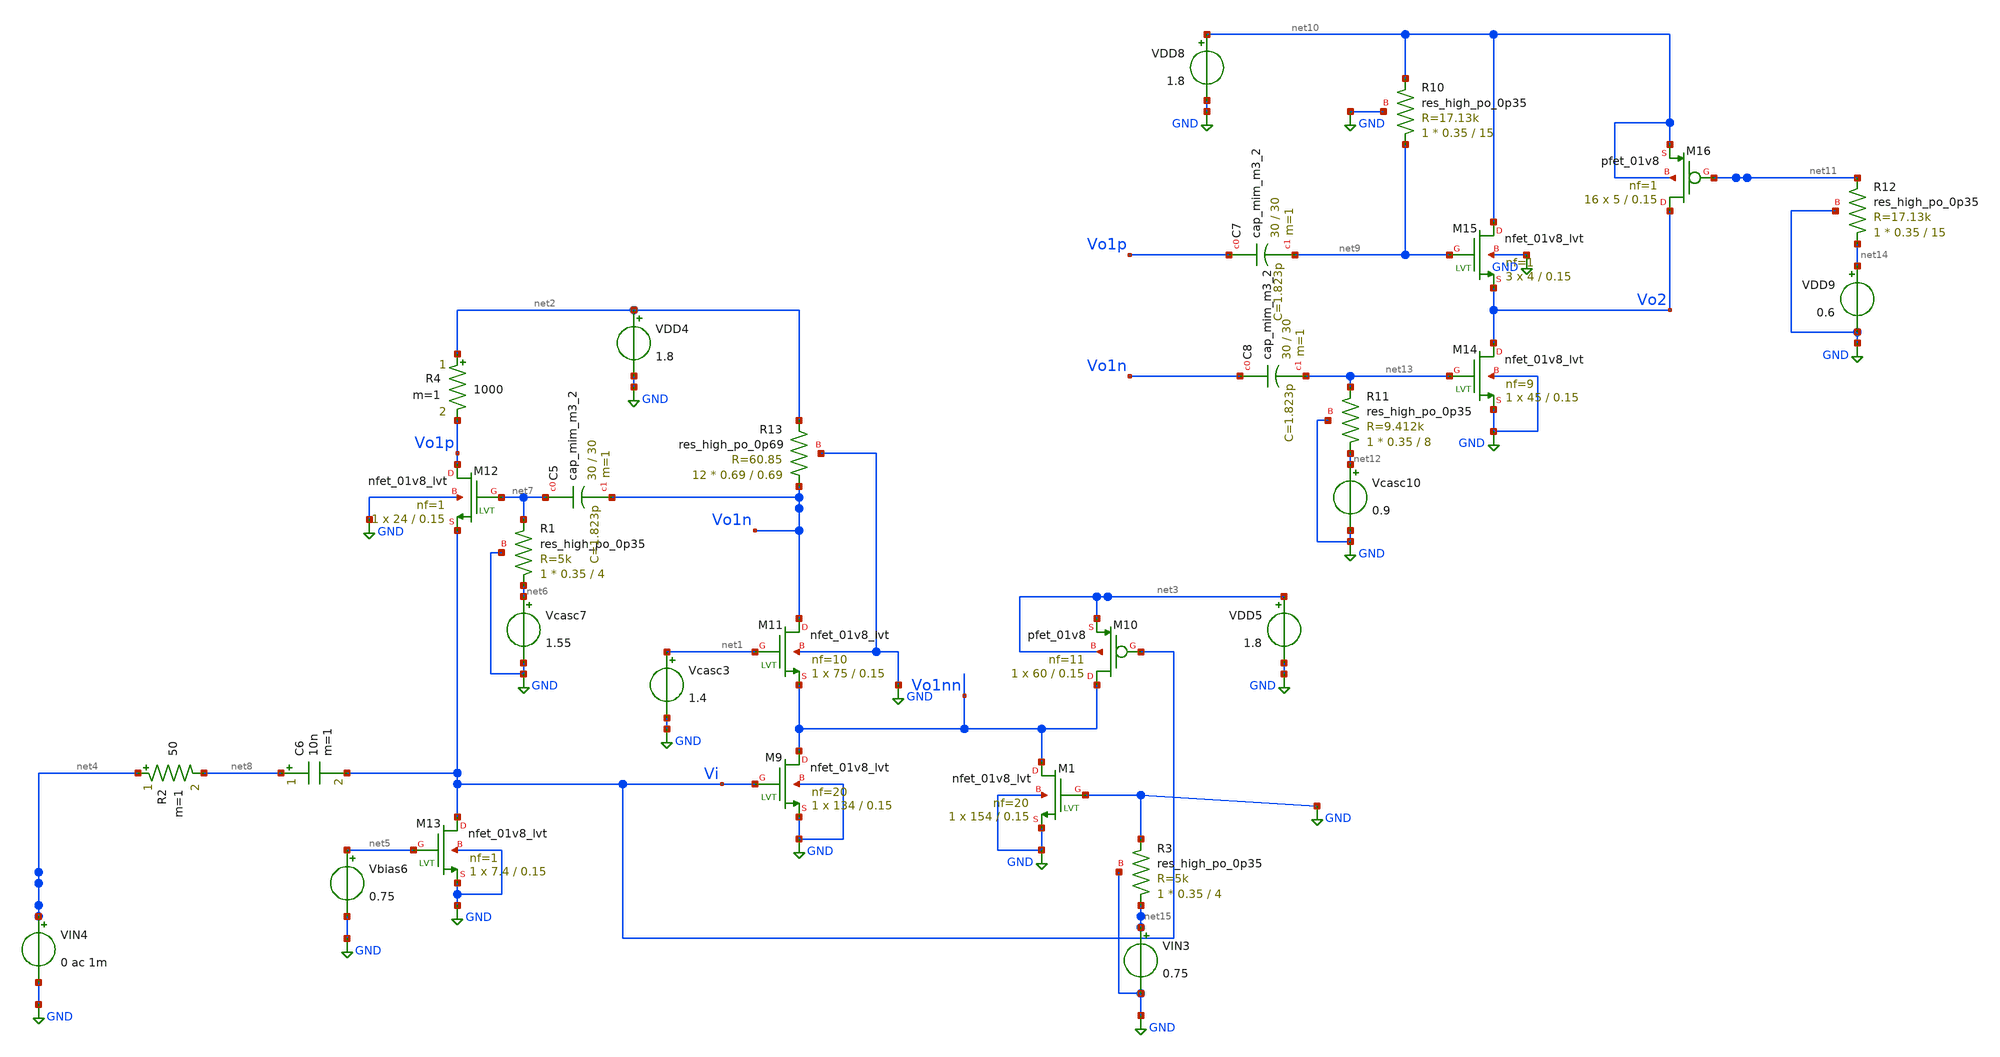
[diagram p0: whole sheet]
** sch_path: xschem/xschem4_sic_final/CompleteAMP6_AC.sch
**.subckt CompleteAMP6_AC
Vcasc3 net1 GND 1.4
VDD4 net2 GND 1.8
VDD5 net3 GND 1.8
Vbias6 net5 GND 0.75
Vcasc7 net6 GND 1.55
XR1 net6 net7 GND sky130_fd_pr__res_high_po_0p35 L=4 mult=1 m=1
XC5 net7 Vo1n sky130_fd_pr__cap_mim_m3_2 W=30 L=30 MF=1 m=1
C6 net8 Vi 10n m=1
XM9 Vo1nn Vi GND GND sky130_fd_pr__nfet_01v8_lvt L=0.15 W=134 nf=20 ad='int((nf+1)/2) * W/nf * 0.29'
+ as='int((nf+2)/2) * W/nf * 0.29' pd='2*int((nf+1)/2) * (W/nf + 0.29)' ps='2*int((nf+2)/2) * (W/nf + 0.29)'
+ nrd='0.29 / W' nrs='0.29 / W' sa=0 sb=0 sd=0 mult=1 m=1
XM10 Vo1nn Vi net3 net3 sky130_fd_pr__pfet_01v8 L=0.15 W=60 nf=11 ad='int((nf+1)/2) * W/nf * 0.29' as='int((nf+2)/2) * W/nf * 0.29'
+ pd='2*int((nf+1)/2) * (W/nf + 0.29)' ps='2*int((nf+2)/2) * (W/nf + 0.29)' nrd='0.29 / W' nrs='0.29 / W'
+ sa=0 sb=0 sd=0 mult=1 m=1
XM11 Vo1n net1 Vo1nn GND sky130_fd_pr__nfet_01v8_lvt L=0.15 W=75 nf=10 ad='int((nf+1)/2) * W/nf * 0.29'
+ as='int((nf+2)/2) * W/nf * 0.29' pd='2*int((nf+1)/2) * (W/nf + 0.29)' ps='2*int((nf+2)/2) * (W/nf + 0.29)'
+ nrd='0.29 / W' nrs='0.29 / W' sa=0 sb=0 sd=0 mult=1 m=1
XM12 Vo1p net7 Vi GND sky130_fd_pr__nfet_01v8_lvt L=0.15 W=24 nf=1 ad='int((nf+1)/2) * W/nf * 0.29' as='int((nf+2)/2) * W/nf * 0.29'
+ pd='2*int((nf+1)/2) * (W/nf + 0.29)' ps='2*int((nf+2)/2) * (W/nf + 0.29)' nrd='0.29 / W' nrs='0.29 / W'
+ sa=0 sb=0 sd=0 mult=1 m=1
XM13 Vi net5 GND GND sky130_fd_pr__nfet_01v8_lvt L=0.15 W=7.4 nf=1 ad='int((nf+1)/2) * W/nf * 0.29' as='int((nf+2)/2) * W/nf * 0.29'
+ pd='2*int((nf+1)/2) * (W/nf + 0.29)' ps='2*int((nf+2)/2) * (W/nf + 0.29)' nrd='0.29 / W' nrs='0.29 / W'
+ sa=0 sb=0 sd=0 mult=1 m=1
XM14 Vo2 net13 GND GND sky130_fd_pr__nfet_01v8_lvt L=0.15 W=45 nf=9 ad='int((nf+1)/2) * W/nf * 0.29'
+ as='int((nf+2)/2) * W/nf * 0.29' pd='2*int((nf+1)/2) * (W/nf + 0.29)' ps='2*int((nf+2)/2) * (W/nf + 0.29)'
+ nrd='0.29 / W' nrs='0.29 / W' sa=0 sb=0 sd=0 mult=1 m=1
XM15 net10 net9 Vo2 GND sky130_fd_pr__nfet_01v8_lvt L=0.15 W=4 nf=1 ad='int((nf+1)/2) * W/nf * 0.29'
+ as='int((nf+2)/2) * W/nf * 0.29' pd='2*int((nf+1)/2) * (W/nf + 0.29)' ps='2*int((nf+2)/2) * (W/nf + 0.29)'
+ nrd='0.29 / W' nrs='0.29 / W' sa=0 sb=0 sd=0 mult=3 m=3
XR10 net9 net10 GND sky130_fd_pr__res_high_po_0p35 L=15 mult=1 m=1
XM16 Vo2 net11 net10 net10 sky130_fd_pr__pfet_01v8 L=0.15 W=5 nf=1 ad='int((nf+1)/2) * W/nf * 0.29' as='int((nf+2)/2) * W/nf * 0.29'
+ pd='2*int((nf+1)/2) * (W/nf + 0.29)' ps='2*int((nf+2)/2) * (W/nf + 0.29)' nrd='0.29 / W' nrs='0.29 / W'
+ sa=0 sb=0 sd=0 mult=16 m=16
VDD8 net10 GND 1.8
VDD9 net14 GND 0.6
XC7 Vo1p net9 sky130_fd_pr__cap_mim_m3_2 W=30 L=30 MF=1 m=1
Vcasc10 net12 GND 0.9
XR11 net12 net13 GND sky130_fd_pr__res_high_po_0p35 L=8 mult=1 m=1
XC8 Vo1n net13 sky130_fd_pr__cap_mim_m3_2 W=30 L=30 MF=1 m=1
XR12 net14 net11 GND sky130_fd_pr__res_high_po_0p35 L=15 mult=1 m=1
XM1 Vo1nn GND GND GND sky130_fd_pr__nfet_01v8_lvt L=0.15 W=154 nf=20 ad='int((nf+1)/2) * W/nf * 0.29'
+ as='int((nf+2)/2) * W/nf * 0.29' pd='2*int((nf+1)/2) * (W/nf + 0.29)' ps='2*int((nf+2)/2) * (W/nf + 0.29)'
+ nrd='0.29 / W' nrs='0.29 / W' sa=0 sb=0 sd=0 mult=1 m=1
VIN3 net15 GND 0.75
XR3 net15 GND GND sky130_fd_pr__res_high_po_0p35 L=4 mult=1 m=1
VIN4 net4 GND 0 ac 1m
XR13 Vo1n net2 GND sky130_fd_pr__res_high_po_0p69 L=0.69 mult=12 m=12
R2 net4 net8 50 m=1
R4 net2 Vo1p 1000 m=1
**** begin user architecture code

.lib $::SKYWATER_MODELS/sky130.lib.spice tt




.control
#tran 1p 5n


print @m.xm9.msky130_fd_pr__nfet_01v8_lvt[id]
print @m.xm1.msky130_fd_pr__nfet_01v8_lvt[id]
print @m.xm10.msky130_fd_pr__pfet_01v8[id]
print @m.xm11.msky130_fd_pr__nfet_01v8_lvt[id]

print @m.xm9.msky130_fd_pr__nfet_01v8_lvt[vth]
print @m.xm1.msky130_fd_pr__nfet_01v8_lvt[vth]
print @m.xm10.msky130_fd_pr__pfet_01v8[vth]
print @m.xm11.msky130_fd_pr__nfet_01v8_lvt[vth]

print @m.xm9.msky130_fd_pr__nfet_01v8_lvt[gm]
print @m.xm1.msky130_fd_pr__nfet_01v8_lvt[gm]
print @m.xm10.msky130_fd_pr__pfet_01v8[gm]
print @m.xm11.msky130_fd_pr__nfet_01v8_lvt[gm]
print @m.xm12.msky130_fd_pr__nfet_01v8_lvt[gm]

#plot v(Vo2)
#plot v(Vo1n)
#plot v(VI) v(VI-)
#plot v(vo1nn)
#spectrum 800MEG 5000MEG 100MEG v(Vo1n)
#let abc=spectrum 800MEG 5000MEG 100MEG v(Vo1n)
#plot db(abc)
ac dec 100 1e9 10e9
plot db(v(Vo2)/v(VI))

let Zo=50;
let Zin=v(vi)/-i(VIN4)
Let S11=mag( (Zin-Zo)/(Zin+Zo) )
plot db(S11)
WRDATA S11.csv db(S11)
plot mag(Zin);ac dec 100 1e9 10e9
plot db(v(Vo1p)/v(VI))
.endc


**** end user architecture code
**.ends
.GLOBAL GND
.end
